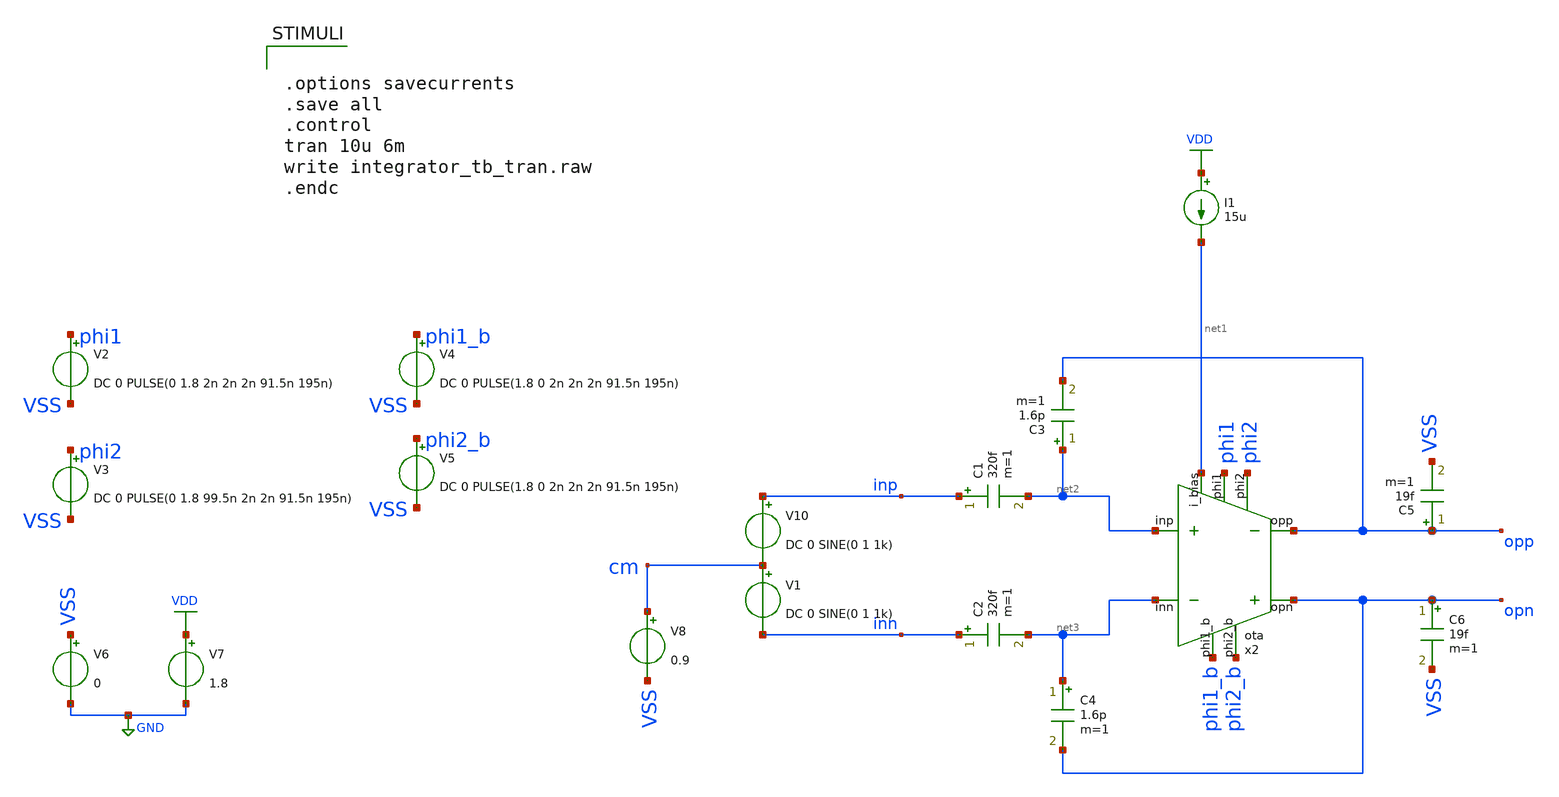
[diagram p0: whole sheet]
** sch_path: verification/schematic/integrator_tb_tran.sch
**.subckt integrator_tb_tran
V6 VSS GND 0
V7 VDD GND 1.8
V8 cm VSS 0.9
V10 inp cm DC 0 SINE(0 1 1k)
V1 cm inn DC 0 SINE(0 1 1k)
V2 phi1 VSS DC 0 PULSE(0 1.8 2n 2n 2n 91.5n 195n)
V3 phi2 VSS DC 0 PULSE(0 1.8 99.5n 2n 2n 91.5n 195n)
V4 phi1_b VSS DC 0 PULSE(1.8 0 2n 2n 2n 91.5n 195n)
V5 phi2_b VSS DC 0 PULSE(1.8 0 2n 2n 2n 91.5n 195n)
x2 net1 net2 net3 phi1 phi1_b phi2 phi2_b opp opn 50 350 VDD VSS ota
I1 VDD net1 15u
C1 inp net2 320f m=1
C2 inn net3 320f m=1
C3 net2 opp 1.6p m=1
C4 net3 opn 1.6p m=1
C5 opp VSS 19f m=1
C6 opn VSS 19f m=1
**** begin user architecture code

** opencircuitdesign pdks install
.lib /farmshare/home/classes/ee/372/PDKs/open_pdks_1.0.310/sky130/sky130A/libs.tech/ngspice/sky130.lib.spice tt



.options savecurrents
.save all
.control
tran 10u 6m
write integrator_tb_tran.raw
.endc


**** end user architecture code
**.ends

* expanding   symbol:  ota.sym # of pins=9
** sym_path: design/schematic/ota.sym
** sch_path: design/schematic/ota.sch
.subckt ota i_bias inp inn phi1 phi1_b phi2 phi2_b opp opn C_CMFB C_COMP VDD VSS  C_CMFB=50
+ C_COMP=350
*.ipin i_bias
*.ipin inp
*.ipin inn
*.ipin phi1
*.ipin phi1_b
*.ipin phi2
*.ipin phi2_b
*.opin opp
*.opin opn
x1 bias_a bias_b bias_c bias_d bias_e i_bias VDD GND folded_cascode_bias
x3 phi1 phi1_b opp opn bias_e bias_a net1 phi2 phi2_b 'C_CMFB' VDD GND sc_cmfb
x2 net1 inp inn bias_a bias_b bias_c bias_d opp opn VDD GND folded_cascode_core_66dB_78degPM
XCcomp1 opp VSS sky130_fd_pr__cap_mim_m3_1 W=1 L=1 MF='C_COMP' m='C_COMP'
XCcomp2 opn VSS sky130_fd_pr__cap_mim_m3_1 W=1 L=1 MF='C_COMP' m='C_COMP'
.ends


* expanding   symbol:  folded_cascode_bias.sym # of pins=6
** sym_path: design/schematic/folded_cascode_bias.sym
** sch_path: design/schematic/folded_cascode_bias.sch
.subckt folded_cascode_bias bias_a bias_b bias_c bias_d bias_e i_bias VDD VSS
*.opin bias_a
*.opin bias_b
*.opin bias_c
*.opin bias_d
*.opin bias_e
*.opin i_bias
XM22 bias_b bias_c net3 VDD sky130_fd_pr__pfet_01v8 L=1 W=1.25 nf=1 ad='int((nf+1)/2) * W/nf * 0.29'
+ as='int((nf+2)/2) * W/nf * 0.29' pd='2*int((nf+1)/2) * (W/nf + 0.29)' ps='2*int((nf+2)/2) * (W/nf + 0.29)'
+ nrd='0.29 / W' nrs='0.29 / W' sa=0 sb=0 sd=0 mult=6 m=6
XM26 net5 bias_c net1 VDD sky130_fd_pr__pfet_01v8 L=1 W=1.25 nf=1 ad='int((nf+1)/2) * W/nf * 0.29' as='int((nf+2)/2) * W/nf * 0.29'
+ pd='2*int((nf+1)/2) * (W/nf + 0.29)' ps='2*int((nf+2)/2) * (W/nf + 0.29)' nrd='0.29 / W' nrs='0.29 / W'
+ sa=0 sb=0 sd=0 mult=6 m=6
XM32 bias_e bias_c net2 VDD sky130_fd_pr__pfet_01v8 L=1 W=1.25 nf=1 ad='int((nf+1)/2) * W/nf * 0.29'
+ as='int((nf+2)/2) * W/nf * 0.29' pd='2*int((nf+1)/2) * (W/nf + 0.29)' ps='2*int((nf+2)/2) * (W/nf + 0.29)'
+ nrd='0.29 / W' nrs='0.29 / W' sa=0 sb=0 sd=0 mult=6 m=6
XM33 bias_e bias_e VSS VSS sky130_fd_pr__nfet_01v8 L=1 W=1.25 nf=1 ad='int((nf+1)/2) * W/nf * 0.29' as='int((nf+2)/2) * W/nf * 0.29'
+ pd='2*int((nf+1)/2) * (W/nf + 0.29)' ps='2*int((nf+2)/2) * (W/nf + 0.29)' nrd='0.29 / W' nrs='0.29 / W'
+ sa=0 sb=0 sd=0 mult=1 m=1
XM21 net3 bias_b VDD VDD sky130_fd_pr__pfet_01v8_lvt L=1 W=1.25 nf=1 ad='int((nf+1)/2) * W/nf * 0.29'
+ as='int((nf+2)/2) * W/nf * 0.29' pd='2*int((nf+1)/2) * (W/nf + 0.29)' ps='2*int((nf+2)/2) * (W/nf + 0.29)'
+ nrd='0.29 / W' nrs='0.29 / W' sa=0 sb=0 sd=0 mult=6 m=6
XM25 net1 bias_b VDD VDD sky130_fd_pr__pfet_01v8_lvt L=1 W=1.25 nf=1 ad='int((nf+1)/2) * W/nf * 0.29'
+ as='int((nf+2)/2) * W/nf * 0.29' pd='2*int((nf+1)/2) * (W/nf + 0.29)' ps='2*int((nf+2)/2) * (W/nf + 0.29)'
+ nrd='0.29 / W' nrs='0.29 / W' sa=0 sb=0 sd=0 mult=6 m=6
XM31 net2 bias_b VDD VDD sky130_fd_pr__pfet_01v8_lvt L=1 W=1.25 nf=1 ad='int((nf+1)/2) * W/nf * 0.29'
+ as='int((nf+2)/2) * W/nf * 0.29' pd='2*int((nf+1)/2) * (W/nf + 0.29)' ps='2*int((nf+2)/2) * (W/nf + 0.29)'
+ nrd='0.29 / W' nrs='0.29 / W' sa=0 sb=0 sd=0 mult=6 m=6
XM1 bias_b bias_b bias_c VSS sky130_fd_pr__nfet_01v8_lvt L=1 W=1.25 nf=1 ad='int((nf+1)/2) * W/nf * 0.29'
+ as='int((nf+2)/2) * W/nf * 0.29' pd='2*int((nf+1)/2) * (W/nf + 0.29)' ps='2*int((nf+2)/2) * (W/nf + 0.29)'
+ nrd='0.29 / W' nrs='0.29 / W' sa=0 sb=0 sd=0 mult=56 m=56
XM2 net5 net5 bias_d VSS sky130_fd_pr__nfet_01v8 L=1 W=1.25 nf=1 ad='int((nf+1)/2) * W/nf * 0.29' as='int((nf+2)/2) * W/nf * 0.29'
+ pd='2*int((nf+1)/2) * (W/nf + 0.29)' ps='2*int((nf+2)/2) * (W/nf + 0.29)' nrd='0.29 / W' nrs='0.29 / W'
+ sa=0 sb=0 sd=0 mult=50 m=50
XM3 bias_d net5 bias_a VSS sky130_fd_pr__nfet_01v8 L=1 W=1.25 nf=1 ad='int((nf+1)/2) * W/nf * 0.29' as='int((nf+2)/2) * W/nf * 0.29'
+ pd='2*int((nf+1)/2) * (W/nf + 0.29)' ps='2*int((nf+2)/2) * (W/nf + 0.29)' nrd='0.29 / W' nrs='0.29 / W'
+ sa=0 sb=0 sd=0 mult=2 m=2
XM4 bias_a bias_d net4 VSS sky130_fd_pr__nfet_01v8 L=1 W=1.25 nf=1 ad='int((nf+1)/2) * W/nf * 0.29' as='int((nf+2)/2) * W/nf * 0.29'
+ pd='2*int((nf+1)/2) * (W/nf + 0.29)' ps='2*int((nf+2)/2) * (W/nf + 0.29)' nrd='0.29 / W' nrs='0.29 / W'
+ sa=0 sb=0 sd=0 mult=18 m=18
XM5 net4 bias_a VSS VSS sky130_fd_pr__nfet_01v8 L=1 W=1.25 nf=1 ad='int((nf+1)/2) * W/nf * 0.29' as='int((nf+2)/2) * W/nf * 0.29'
+ pd='2*int((nf+1)/2) * (W/nf + 0.29)' ps='2*int((nf+2)/2) * (W/nf + 0.29)' nrd='0.29 / W' nrs='0.29 / W'
+ sa=0 sb=0 sd=0 mult=18 m=18
XM6 bias_c i_bias VSS VSS sky130_fd_pr__nfet_01v8 L=1 W=1.25 nf=1 ad='int((nf+1)/2) * W/nf * 0.29' as='int((nf+2)/2) * W/nf * 0.29'
+ pd='2*int((nf+1)/2) * (W/nf + 0.29)' ps='2*int((nf+2)/2) * (W/nf + 0.29)' nrd='0.29 / W' nrs='0.29 / W'
+ sa=0 sb=0 sd=0 mult=18 m=18
XM7 i_bias i_bias VSS VSS sky130_fd_pr__nfet_01v8 L=1 W=1.25 nf=1 ad='int((nf+1)/2) * W/nf * 0.29' as='int((nf+2)/2) * W/nf * 0.29'
+ pd='2*int((nf+1)/2) * (W/nf + 0.29)' ps='2*int((nf+2)/2) * (W/nf + 0.29)' nrd='0.29 / W' nrs='0.29 / W'
+ sa=0 sb=0 sd=0 mult=18 m=18
.ends


* expanding   symbol:  sc_cmfb.sym # of pins=9
** sym_path: design/schematic/sc_cmfb.sym
** sch_path: design/schematic/sc_cmfb.sch
.subckt sc_cmfb phi1 phi1_b opp opn cm bias_a cmc phi2 phi2_b MF VDD VSS  MF=50
*.ipin opn
*.ipin cm
*.ipin bias_a
*.ipin opp
*.opin cmc
*.ipin phi2_b
*.ipin phi2
*.ipin phi1_b
*.ipin phi1
x1 net1 cm phi1 phi1_b VDD GND 1 5.3 0.15 13.7 0.15 transmission_gate
x2 net2 bias_a phi1 phi1_b VDD GND 1 5.3 0.15 13.7 0.15 transmission_gate
x3 net3 cm phi1 phi1_b VDD GND 1 5.3 0.15 13.7 0.15 transmission_gate
x4 opp net1 phi2 phi2_b VDD GND 1 5.3 0.15 13.7 0.15 transmission_gate
x5 cmc net2 phi2 phi2_b VDD GND 1 5.3 0.15 13.7 0.15 transmission_gate
x6 opn net3 phi2 phi2_b VDD GND 1 5.3 0.15 13.7 0.15 transmission_gate
XC1 net1 net2 sky130_fd_pr__cap_mim_m3_1 W=1 L=1 MF='MF' m='MF'
XC2 net2 net3 sky130_fd_pr__cap_mim_m3_1 W=1 L=1 MF='MF' m='MF'
XC3 opp cmc sky130_fd_pr__cap_mim_m3_1 W=1 L=1 MF='MF' m='MF'
XC4 cmc opn sky130_fd_pr__cap_mim_m3_1 W=1 L=1 MF='MF' m='MF'
.ends


* expanding   symbol:  folded_cascode_core_66dB_78degPM.sym # of pins=9
** sym_path: design/schematic/folded_cascode_core_66dB_78degPM.sym
** sch_path: design/schematic/folded_cascode_core_66dB_78degPM.sch
.subckt folded_cascode_core_66dB_78degPM cmc inp inn bias_a bias_b bias_c bias_d opp opn VDD VSS
*.ipin cmc
*.ipin inp
*.ipin inn
*.ipin bias_a
*.ipin bias_b
*.ipin bias_c
*.ipin bias_d
*.opin opp
*.opin opn
XM1 net2 inp net1 VSS sky130_fd_pr__nfet_01v8_lvt L=0.2 W=1.2 nf=1 ad='int((nf+1)/2) * W/nf * 0.29' as='int((nf+2)/2) * W/nf * 0.29'
+ pd='2*int((nf+1)/2) * (W/nf + 0.29)' ps='2*int((nf+2)/2) * (W/nf + 0.29)' nrd='0.29 / W' nrs='0.29 / W'
+ sa=0 sb=0 sd=0 mult=18 m=18
XM2 net3 inn net1 VSS sky130_fd_pr__nfet_01v8_lvt L=0.2 W=1.2 nf=1 ad='int((nf+1)/2) * W/nf * 0.29' as='int((nf+2)/2) * W/nf * 0.29'
+ pd='2*int((nf+1)/2) * (W/nf + 0.29)' ps='2*int((nf+2)/2) * (W/nf + 0.29)' nrd='0.29 / W' nrs='0.29 / W'
+ sa=0 sb=0 sd=0 mult=18 m=18
XM6 net1 cmc VSS VSS sky130_fd_pr__nfet_01v8 L=1 W=1.25 nf=1 ad='int((nf+1)/2) * W/nf * 0.29' as='int((nf+2)/2) * W/nf * 0.29'
+ pd='2*int((nf+1)/2) * (W/nf + 0.29)' ps='2*int((nf+2)/2) * (W/nf + 0.29)' nrd='0.29 / W' nrs='0.29 / W'
+ sa=0 sb=0 sd=0 mult=36 m=36
XM5 net1 bias_a VSS VSS sky130_fd_pr__nfet_01v8 L=1 W=1.25 nf=1 ad='int((nf+1)/2) * W/nf * 0.29' as='int((nf+2)/2) * W/nf * 0.29'
+ pd='2*int((nf+1)/2) * (W/nf + 0.29)' ps='2*int((nf+2)/2) * (W/nf + 0.29)' nrd='0.29 / W' nrs='0.29 / W'
+ sa=0 sb=0 sd=0 mult=36 m=36
XM11 net2 bias_b VDD VDD sky130_fd_pr__pfet_01v8_lvt L=1 W=1.25 nf=1 ad='int((nf+1)/2) * W/nf * 0.29'
+ as='int((nf+2)/2) * W/nf * 0.29' pd='2*int((nf+1)/2) * (W/nf + 0.29)' ps='2*int((nf+2)/2) * (W/nf + 0.29)'
+ nrd='0.29 / W' nrs='0.29 / W' sa=0 sb=0 sd=0 mult=12 m=12
XM12 net3 bias_b VDD VDD sky130_fd_pr__pfet_01v8_lvt L=1 W=1.25 nf=1 ad='int((nf+1)/2) * W/nf * 0.29'
+ as='int((nf+2)/2) * W/nf * 0.29' pd='2*int((nf+1)/2) * (W/nf + 0.29)' ps='2*int((nf+2)/2) * (W/nf + 0.29)'
+ nrd='0.29 / W' nrs='0.29 / W' sa=0 sb=0 sd=0 mult=12 m=12
XM1A opn bias_c net2 VDD sky130_fd_pr__pfet_01v8 L=1 W=1.25 nf=1 ad='int((nf+1)/2) * W/nf * 0.29' as='int((nf+2)/2) * W/nf * 0.29'
+ pd='2*int((nf+1)/2) * (W/nf + 0.29)' ps='2*int((nf+2)/2) * (W/nf + 0.29)' nrd='0.29 / W' nrs='0.29 / W'
+ sa=0 sb=0 sd=0 mult=18 m=18
XM8 opp bias_c net3 VDD sky130_fd_pr__pfet_01v8 L=1 W=1.25 nf=1 ad='int((nf+1)/2) * W/nf * 0.29' as='int((nf+2)/2) * W/nf * 0.29'
+ pd='2*int((nf+1)/2) * (W/nf + 0.29)' ps='2*int((nf+2)/2) * (W/nf + 0.29)' nrd='0.29 / W' nrs='0.29 / W'
+ sa=0 sb=0 sd=0 mult=18 m=18
XM3A opn bias_d net4 VSS sky130_fd_pr__nfet_01v8 L=1 W=1.25 nf=1 ad='int((nf+1)/2) * W/nf * 0.29' as='int((nf+2)/2) * W/nf * 0.29'
+ pd='2*int((nf+1)/2) * (W/nf + 0.29)' ps='2*int((nf+2)/2) * (W/nf + 0.29)' nrd='0.29 / W' nrs='0.29 / W'
+ sa=0 sb=0 sd=0 mult=18 m=18
XM7 opp bias_d net5 VSS sky130_fd_pr__nfet_01v8 L=1 W=1.25 nf=1 ad='int((nf+1)/2) * W/nf * 0.29' as='int((nf+2)/2) * W/nf * 0.29'
+ pd='2*int((nf+1)/2) * (W/nf + 0.29)' ps='2*int((nf+2)/2) * (W/nf + 0.29)' nrd='0.29 / W' nrs='0.29 / W'
+ sa=0 sb=0 sd=0 mult=18 m=18
XM3 net4 bias_a VSS VSS sky130_fd_pr__nfet_01v8 L=1 W=1.25 nf=1 ad='int((nf+1)/2) * W/nf * 0.29' as='int((nf+2)/2) * W/nf * 0.29'
+ pd='2*int((nf+1)/2) * (W/nf + 0.29)' ps='2*int((nf+2)/2) * (W/nf + 0.29)' nrd='0.29 / W' nrs='0.29 / W'
+ sa=0 sb=0 sd=0 mult=18 m=18
XM4 net5 bias_a VSS VSS sky130_fd_pr__nfet_01v8 L=1 W=1.25 nf=1 ad='int((nf+1)/2) * W/nf * 0.29' as='int((nf+2)/2) * W/nf * 0.29'
+ pd='2*int((nf+1)/2) * (W/nf + 0.29)' ps='2*int((nf+2)/2) * (W/nf + 0.29)' nrd='0.29 / W' nrs='0.29 / W'
+ sa=0 sb=0 sd=0 mult=18 m=18
.ends


* expanding   symbol:  transmission_gate.sym # of pins=4
** sym_path: design/schematic/transmission_gate.sym
** sch_path: design/schematic/transmission_gate.sch
.subckt transmission_gate in out en en_b VDD VSS N W_N L_N W_P L_P    N=1 W_N=5.3 L_N=0.15 W_P=13.7
+ L_P=0.15
*.iopin in
*.iopin out
*.ipin en
*.ipin en_b
XM1 out en in VSS sky130_fd_pr__nfet_01v8 L=L_N W=W_N nf=1 ad='int((nf+1)/2) * W/nf * 0.29' as='int((nf+2)/2) * W/nf * 0.29'
+ pd='2*int((nf+1)/2) * (W/nf + 0.29)' ps='2*int((nf+2)/2) * (W/nf + 0.29)' nrd='0.29 / W' nrs='0.29 / W'
+ sa=0 sb=0 sd=0 mult=N m=N
XM2 out en_b in VDD sky130_fd_pr__pfet_01v8 L=L_P W=W_P nf=1 ad='int((nf+1)/2) * W/nf * 0.29' as='int((nf+2)/2) * W/nf * 0.29'
+ pd='2*int((nf+1)/2) * (W/nf + 0.29)' ps='2*int((nf+2)/2) * (W/nf + 0.29)' nrd='0.29 / W' nrs='0.29 / W'
+ sa=0 sb=0 sd=0 mult=N m=N
.ends

.GLOBAL VDD
.GLOBAL GND
.end
